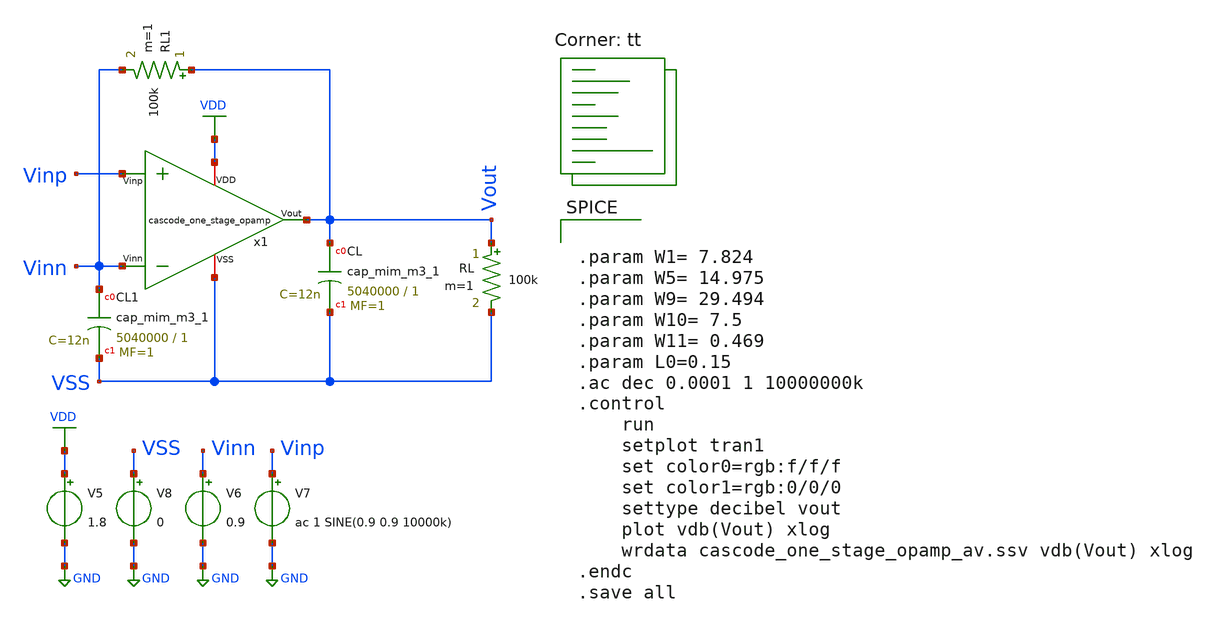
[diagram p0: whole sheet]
** sch_path: opamp_design/cascode_one_stage_opamp/cascode_one_stage_opamp_av.sch
**.subckt cascode_one_stage_opamp_av
XCL Vout VSS sky130_fd_pr__cap_mim_m3_1 W=5040000 L=1 MF=1 m=1
RL Vout VSS 100k m=1
XCL1 Vinn VSS sky130_fd_pr__cap_mim_m3_1 W=5040000 L=1 MF=1 m=1
RL1 Vout Vinn 100k m=1
V5 VDD GND 1.8
V6 Vinn GND 0.9
V7 Vinp GND ac 1 SINE(0.9 0.9 10000k)
V8 VSS GND 0
x1 VDD Vout Vinp Vinn VSS cascode_one_stage_opamp
**** begin user architecture code
.lib $::SKYWATER_MODELS/sky130.lib.spice tt


.param W1= 7.824
.param W5= 14.975
.param W9= 29.494
.param W10= 7.5
.param W11= 0.469
.param L0=0.15
.ac dec 0.0001 1 10000000k
.control
	run
	setplot tran1
	set color0=rgb:f/f/f
	set color1=rgb:0/0/0
	settype decibel vout
	plot vdb(Vout) xlog
	wrdata cascode_one_stage_opamp_av.ssv vdb(Vout) xlog
.endc
.save all


**** end user architecture code
**.ends

* expanding   symbol:
*+  /home/ricardo/RATT_repos/Proyectos_xschem/opamp_design/cascode_one_stage_opamp/cascode_one_stage_opamp.sym # of pins=5
** sym_path: opamp_design/cascode_one_stage_opamp/cascode_one_stage_opamp.sym
** sch_path: opamp_design/cascode_one_stage_opamp/cascode_one_stage_opamp.sch
.subckt cascode_one_stage_opamp VDD Vout Vinp Vinn VSS
*.ipin Vinp
*.ipin Vinn
*.opin Vout
*.iopin VDD
*.iopin VSS
XM1 net6 Vinp net1 VSS sky130_fd_pr__nfet_01v8 L={L0} W={W1} nf=1 ad='int((nf+1)/2) * W/nf * 0.29' as='int((nf+2)/2) * W/nf * 0.29'
+ pd='2*int((nf+1)/2) * (W/nf + 0.29)' ps='2*int((nf+2)/2) * (W/nf + 0.29)' nrd='0.29 / W' nrs='0.29 / W'
+ sa=0 sb=0 sd=0 mult=1 m=1
XM2 net7 Vinn net1 VSS sky130_fd_pr__nfet_01v8 L={L0} W={W1} nf=1 ad='int((nf+1)/2) * W/nf * 0.29' as='int((nf+2)/2) * W/nf * 0.29'
+ pd='2*int((nf+1)/2) * (W/nf + 0.29)' ps='2*int((nf+2)/2) * (W/nf + 0.29)' nrd='0.29 / W' nrs='0.29 / W'
+ sa=0 sb=0 sd=0 mult=1 m=1
XM9 net1 net9 VSS VSS sky130_fd_pr__nfet_01v8 L={L0} W={W9} nf=1 ad='int((nf+1)/2) * W/nf * 0.29' as='int((nf+2)/2) * W/nf * 0.29'
+ pd='2*int((nf+1)/2) * (W/nf + 0.29)' ps='2*int((nf+2)/2) * (W/nf + 0.29)' nrd='0.29 / W' nrs='0.29 / W'
+ sa=0 sb=0 sd=0 mult=1 m=1
XM11 net2 net2 net1 VSS sky130_fd_pr__nfet_01v8 L={L0} W={W11} nf=1 ad='int((nf+1)/2) * W/nf * 0.29'
+ as='int((nf+2)/2) * W/nf * 0.29' pd='2*int((nf+1)/2) * (W/nf + 0.29)' ps='2*int((nf+2)/2) * (W/nf + 0.29)'
+ nrd='0.29 / W' nrs='0.29 / W' sa=0 sb=0 sd=0 mult=1 m=1
XM3 net3 net2 net6 VSS sky130_fd_pr__nfet_01v8 L={L0} W={W1} nf=1 ad='int((nf+1)/2) * W/nf * 0.29' as='int((nf+2)/2) * W/nf * 0.29'
+ pd='2*int((nf+1)/2) * (W/nf + 0.29)' ps='2*int((nf+2)/2) * (W/nf + 0.29)' nrd='0.29 / W' nrs='0.29 / W'
+ sa=0 sb=0 sd=0 mult=1 m=1
XM4 Vout net2 net7 VSS sky130_fd_pr__nfet_01v8 L={L0} W={W1} nf=1 ad='int((nf+1)/2) * W/nf * 0.29' as='int((nf+2)/2) * W/nf * 0.29'
+ pd='2*int((nf+1)/2) * (W/nf + 0.29)' ps='2*int((nf+2)/2) * (W/nf + 0.29)' nrd='0.29 / W' nrs='0.29 / W'
+ sa=0 sb=0 sd=0 mult=1 m=1
XM6 Vout net8 net4 VDD sky130_fd_pr__pfet_01v8 L={L0} W={W5} nf=1 ad='int((nf+1)/2) * W/nf * 0.29' as='int((nf+2)/2) * W/nf * 0.29'
+ pd='2*int((nf+1)/2) * (W/nf + 0.29)' ps='2*int((nf+2)/2) * (W/nf + 0.29)' nrd='0.29 / W' nrs='0.29 / W'
+ sa=0 sb=0 sd=0 mult=1 m=1
XM5 net3 net8 net5 VDD sky130_fd_pr__pfet_01v8 L={L0} W={W5} nf=1 ad='int((nf+1)/2) * W/nf * 0.29' as='int((nf+2)/2) * W/nf * 0.29'
+ pd='2*int((nf+1)/2) * (W/nf + 0.29)' ps='2*int((nf+2)/2) * (W/nf + 0.29)' nrd='0.29 / W' nrs='0.29 / W'
+ sa=0 sb=0 sd=0 mult=1 m=1
XM7 net5 net3 VDD VDD sky130_fd_pr__pfet_01v8 L={L0} W={W5} nf=1 ad='int((nf+1)/2) * W/nf * 0.29' as='int((nf+2)/2) * W/nf * 0.29'
+ pd='2*int((nf+1)/2) * (W/nf + 0.29)' ps='2*int((nf+2)/2) * (W/nf + 0.29)' nrd='0.29 / W' nrs='0.29 / W'
+ sa=0 sb=0 sd=0 mult=1 m=1
XM8 net4 net3 VDD VDD sky130_fd_pr__pfet_01v8 L={L0} W={W5} nf=1 ad='int((nf+1)/2) * W/nf * 0.29' as='int((nf+2)/2) * W/nf * 0.29'
+ pd='2*int((nf+1)/2) * (W/nf + 0.29)' ps='2*int((nf+2)/2) * (W/nf + 0.29)' nrd='0.29 / W' nrs='0.29 / W'
+ sa=0 sb=0 sd=0 mult=1 m=1
XM10 net2 net10 VDD VDD sky130_fd_pr__pfet_01v8 L={L0} W={W10} nf=1 ad='int((nf+1)/2) * W/nf * 0.29'
+ as='int((nf+2)/2) * W/nf * 0.29' pd='2*int((nf+1)/2) * (W/nf + 0.29)' ps='2*int((nf+2)/2) * (W/nf + 0.29)'
+ nrd='0.29 / W' nrs='0.29 / W' sa=0 sb=0 sd=0 mult=1 m=1
XM14 net9 net9 VSS VSS sky130_fd_pr__nfet_01v8 L={L0} W={W9} nf=1 ad='int((nf+1)/2) * W/nf * 0.29' as='int((nf+2)/2) * W/nf * 0.29'
+ pd='2*int((nf+1)/2) * (W/nf + 0.29)' ps='2*int((nf+2)/2) * (W/nf + 0.29)' nrd='0.29 / W' nrs='0.29 / W'
+ sa=0 sb=0 sd=0 mult=1 m=1
I0 VDD net9 100u
I1 net10 VSS 12u
XM12 net10 net10 VDD VDD sky130_fd_pr__pfet_01v8 L={L0} W={W10} nf=1 ad='int((nf+1)/2) * W/nf * 0.29'
+ as='int((nf+2)/2) * W/nf * 0.29' pd='2*int((nf+1)/2) * (W/nf + 0.29)' ps='2*int((nf+2)/2) * (W/nf + 0.29)'
+ nrd='0.29 / W' nrs='0.29 / W' sa=0 sb=0 sd=0 mult=1 m=1
I2 net8 VSS 50u
XM13 net8 net8 VDD VDD sky130_fd_pr__pfet_01v8 L={L0} W={W5} nf=1 ad='int((nf+1)/2) * W/nf * 0.29' as='int((nf+2)/2) * W/nf * 0.29'
+ pd='2*int((nf+1)/2) * (W/nf + 0.29)' ps='2*int((nf+2)/2) * (W/nf + 0.29)' nrd='0.29 / W' nrs='0.29 / W'
+ sa=0 sb=0 sd=0 mult=1 m=1
.ends

.GLOBAL VDD
.GLOBAL GND
.end
